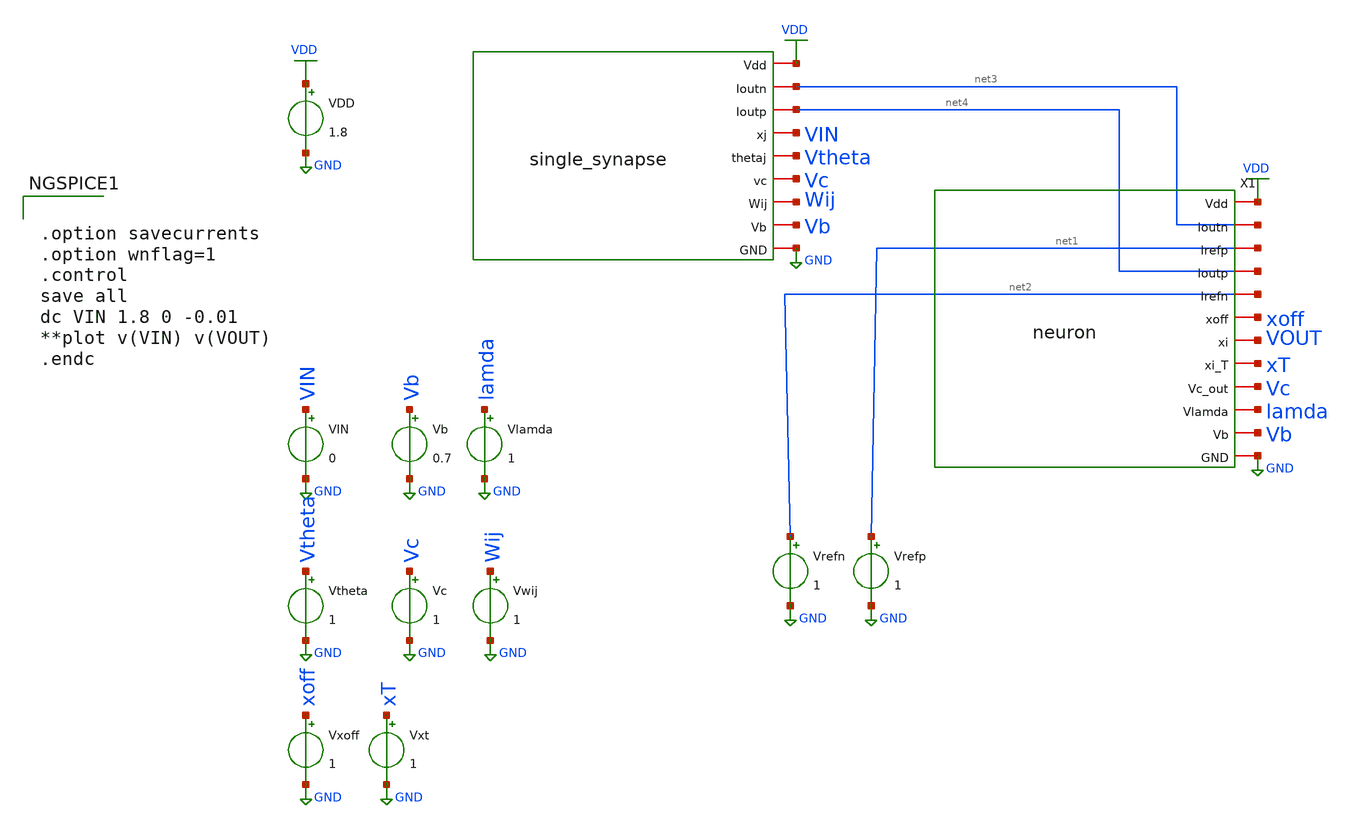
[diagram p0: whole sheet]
** sch_path: synapse_neuron_test.sch
**.subckt synapse_neuron_test
x1 VDD net3 net4 VIN Vtheta Vc Wij Vb GND single_synapse
VDD VDD GND 1.8
VIN VIN GND 0
Vb Vb GND 0.7
Vtheta Vtheta GND 1
Vc Vc GND 1
Vwij Wij GND 1
Vrefn net2 GND 1
Vrefp net1 GND 1
Vlamda lamda GND 1
Vxoff xoff GND 1
Vxt xT GND 1
X1 VDD net3 net1 net4 net2 xoff VOUT xT Vc lamda Vb GND neuron
**** begin user architecture code


.option savecurrents
.option wnflag=1
.control
save all
dc VIN 1.8 0 -0.01
**plot v(VIN) v(VOUT)
.endc



** opencircuitdesign pdks install
.lib $::SKYWATER_MODELS/sky130.lib.spice tt


**** end user architecture code
**.ends
.GLOBAL GND
.GLOBAL VDD
.end
